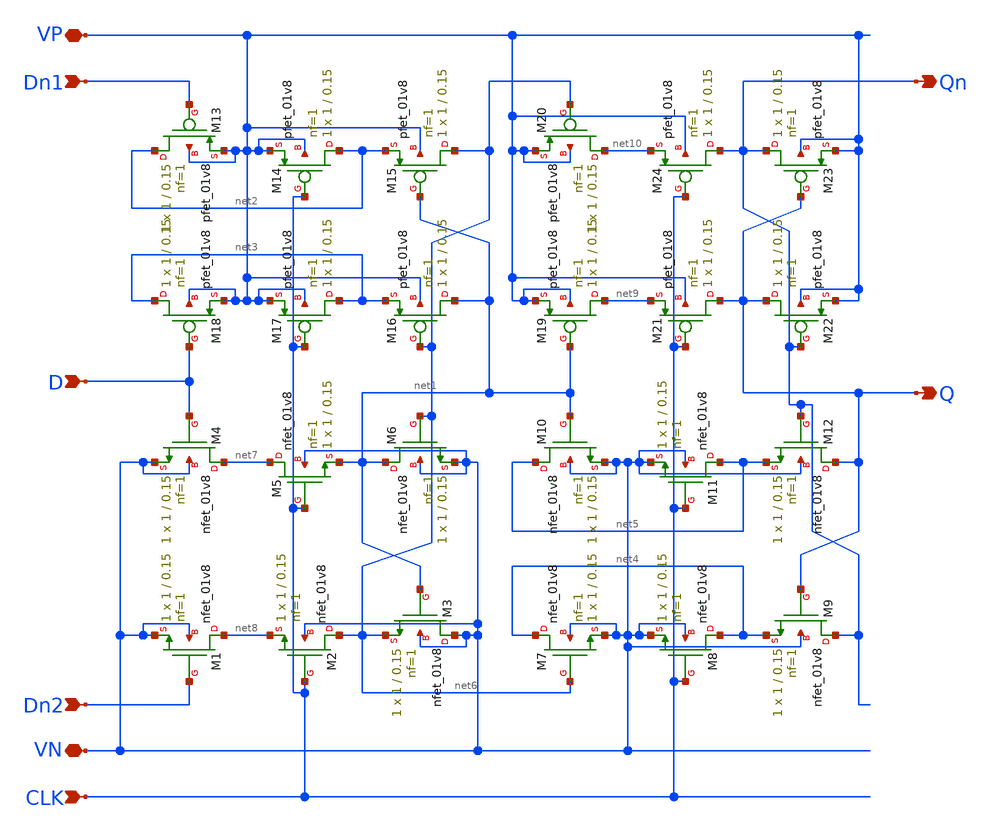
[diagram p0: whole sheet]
** sch_path: projects/negdff/xschem_ngspice/negdff2.sch
**.subckt negdff2 D Dn1 Dn2 Q Qn CLK VP VN
*.ipin D
*.ipin Dn1
*.ipin Dn2
*.opin Q
*.opin Qn
*.ipin CLK
*.iopin VP
*.iopin VN
XM1 net8 Dn2 VN VN sky130_fd_pr__nfet_01v8 L=0.15 W=1 nf=1 ad='int((nf+1)/2) * W/nf * 0.29' as='int((nf+2)/2) * W/nf * 0.29'
+ pd='2*int((nf+1)/2) * (W/nf + 0.29)' ps='2*int((nf+2)/2) * (W/nf + 0.29)' nrd='0.29 / W' nrs='0.29 / W'
+ sa=0 sb=0 sd=0 mult=1 m=1
XM2 net6 CLK net8 VN sky130_fd_pr__nfet_01v8 L=0.15 W=1 nf=1 ad='int((nf+1)/2) * W/nf * 0.29' as='int((nf+2)/2) * W/nf * 0.29'
+ pd='2*int((nf+1)/2) * (W/nf + 0.29)' ps='2*int((nf+2)/2) * (W/nf + 0.29)' nrd='0.29 / W' nrs='0.29 / W'
+ sa=0 sb=0 sd=0 mult=1 m=1
XM3 VN net1 net6 VN sky130_fd_pr__nfet_01v8 L=0.15 W=1 nf=1 ad='int((nf+1)/2) * W/nf * 0.29' as='int((nf+2)/2) * W/nf * 0.29'
+ pd='2*int((nf+1)/2) * (W/nf + 0.29)' ps='2*int((nf+2)/2) * (W/nf + 0.29)' nrd='0.29 / W' nrs='0.29 / W'
+ sa=0 sb=0 sd=0 mult=1 m=1
XM4 net7 D VN VN sky130_fd_pr__nfet_01v8 L=0.15 W=1 nf=1 ad='int((nf+1)/2) * W/nf * 0.29' as='int((nf+2)/2) * W/nf * 0.29'
+ pd='2*int((nf+1)/2) * (W/nf + 0.29)' ps='2*int((nf+2)/2) * (W/nf + 0.29)' nrd='0.29 / W' nrs='0.29 / W'
+ sa=0 sb=0 sd=0 mult=1 m=1
XM5 net7 CLK net1 VN sky130_fd_pr__nfet_01v8 L=0.15 W=1 nf=1 ad='int((nf+1)/2) * W/nf * 0.29' as='int((nf+2)/2) * W/nf * 0.29'
+ pd='2*int((nf+1)/2) * (W/nf + 0.29)' ps='2*int((nf+2)/2) * (W/nf + 0.29)' nrd='0.29 / W' nrs='0.29 / W'
+ sa=0 sb=0 sd=0 mult=1 m=1
XM6 net1 net6 VN VN sky130_fd_pr__nfet_01v8 L=0.15 W=1 nf=1 ad='int((nf+1)/2) * W/nf * 0.29' as='int((nf+2)/2) * W/nf * 0.29'
+ pd='2*int((nf+1)/2) * (W/nf + 0.29)' ps='2*int((nf+2)/2) * (W/nf + 0.29)' nrd='0.29 / W' nrs='0.29 / W'
+ sa=0 sb=0 sd=0 mult=1 m=1
XM7 net4 net6 VN VN sky130_fd_pr__nfet_01v8 L=0.15 W=1 nf=1 ad='int((nf+1)/2) * W/nf * 0.29' as='int((nf+2)/2) * W/nf * 0.29'
+ pd='2*int((nf+1)/2) * (W/nf + 0.29)' ps='2*int((nf+2)/2) * (W/nf + 0.29)' nrd='0.29 / W' nrs='0.29 / W'
+ sa=0 sb=0 sd=0 mult=1 m=1
XM8 net4 CLK VN VN sky130_fd_pr__nfet_01v8 L=0.15 W=1 nf=1 ad='int((nf+1)/2) * W/nf * 0.29' as='int((nf+2)/2) * W/nf * 0.29'
+ pd='2*int((nf+1)/2) * (W/nf + 0.29)' ps='2*int((nf+2)/2) * (W/nf + 0.29)' nrd='0.29 / W' nrs='0.29 / W'
+ sa=0 sb=0 sd=0 mult=1 m=1
XM9 Qn Q net4 VN sky130_fd_pr__nfet_01v8 L=0.15 W=1 nf=1 ad='int((nf+1)/2) * W/nf * 0.29' as='int((nf+2)/2) * W/nf * 0.29'
+ pd='2*int((nf+1)/2) * (W/nf + 0.29)' ps='2*int((nf+2)/2) * (W/nf + 0.29)' nrd='0.29 / W' nrs='0.29 / W'
+ sa=0 sb=0 sd=0 mult=1 m=1
XM10 net5 net1 VN VN sky130_fd_pr__nfet_01v8 L=0.15 W=1 nf=1 ad='int((nf+1)/2) * W/nf * 0.29' as='int((nf+2)/2) * W/nf * 0.29'
+ pd='2*int((nf+1)/2) * (W/nf + 0.29)' ps='2*int((nf+2)/2) * (W/nf + 0.29)' nrd='0.29 / W' nrs='0.29 / W'
+ sa=0 sb=0 sd=0 mult=1 m=1
XM11 net5 CLK VN VN sky130_fd_pr__nfet_01v8 L=0.15 W=1 nf=1 ad='int((nf+1)/2) * W/nf * 0.29' as='int((nf+2)/2) * W/nf * 0.29'
+ pd='2*int((nf+1)/2) * (W/nf + 0.29)' ps='2*int((nf+2)/2) * (W/nf + 0.29)' nrd='0.29 / W' nrs='0.29 / W'
+ sa=0 sb=0 sd=0 mult=1 m=1
XM12 Q Qn net5 VN sky130_fd_pr__nfet_01v8 L=0.15 W=1 nf=1 ad='int((nf+1)/2) * W/nf * 0.29' as='int((nf+2)/2) * W/nf * 0.29'
+ pd='2*int((nf+1)/2) * (W/nf + 0.29)' ps='2*int((nf+2)/2) * (W/nf + 0.29)' nrd='0.29 / W' nrs='0.29 / W'
+ sa=0 sb=0 sd=0 mult=1 m=1
XM13 net2 Dn1 VP VP sky130_fd_pr__pfet_01v8 L=0.15 W=1 nf=1 ad='int((nf+1)/2) * W/nf * 0.29' as='int((nf+2)/2) * W/nf * 0.29'
+ pd='2*int((nf+1)/2) * (W/nf + 0.29)' ps='2*int((nf+2)/2) * (W/nf + 0.29)' nrd='0.29 / W' nrs='0.29 / W'
+ sa=0 sb=0 sd=0 mult=1 m=1
XM14 net2 CLK VP VP sky130_fd_pr__pfet_01v8 L=0.15 W=1 nf=1 ad='int((nf+1)/2) * W/nf * 0.29' as='int((nf+2)/2) * W/nf * 0.29'
+ pd='2*int((nf+1)/2) * (W/nf + 0.29)' ps='2*int((nf+2)/2) * (W/nf + 0.29)' nrd='0.29 / W' nrs='0.29 / W'
+ sa=0 sb=0 sd=0 mult=1 m=1
XM15 net6 net1 net2 VP sky130_fd_pr__pfet_01v8 L=0.15 W=1 nf=1 ad='int((nf+1)/2) * W/nf * 0.29' as='int((nf+2)/2) * W/nf * 0.29'
+ pd='2*int((nf+1)/2) * (W/nf + 0.29)' ps='2*int((nf+2)/2) * (W/nf + 0.29)' nrd='0.29 / W' nrs='0.29 / W'
+ sa=0 sb=0 sd=0 mult=1 m=1
XM16 net1 net6 net3 VP sky130_fd_pr__pfet_01v8 L=0.15 W=1 nf=1 ad='int((nf+1)/2) * W/nf * 0.29' as='int((nf+2)/2) * W/nf * 0.29'
+ pd='2*int((nf+1)/2) * (W/nf + 0.29)' ps='2*int((nf+2)/2) * (W/nf + 0.29)' nrd='0.29 / W' nrs='0.29 / W'
+ sa=0 sb=0 sd=0 mult=1 m=1
XM17 net3 CLK VP VP sky130_fd_pr__pfet_01v8 L=0.15 W=1 nf=1 ad='int((nf+1)/2) * W/nf * 0.29' as='int((nf+2)/2) * W/nf * 0.29'
+ pd='2*int((nf+1)/2) * (W/nf + 0.29)' ps='2*int((nf+2)/2) * (W/nf + 0.29)' nrd='0.29 / W' nrs='0.29 / W'
+ sa=0 sb=0 sd=0 mult=1 m=1
XM18 net3 D VP VP sky130_fd_pr__pfet_01v8 L=0.15 W=1 nf=1 ad='int((nf+1)/2) * W/nf * 0.29' as='int((nf+2)/2) * W/nf * 0.29'
+ pd='2*int((nf+1)/2) * (W/nf + 0.29)' ps='2*int((nf+2)/2) * (W/nf + 0.29)' nrd='0.29 / W' nrs='0.29 / W'
+ sa=0 sb=0 sd=0 mult=1 m=1
XM19 net9 net1 VP VP sky130_fd_pr__pfet_01v8 L=0.15 W=1 nf=1 ad='int((nf+1)/2) * W/nf * 0.29' as='int((nf+2)/2) * W/nf * 0.29'
+ pd='2*int((nf+1)/2) * (W/nf + 0.29)' ps='2*int((nf+2)/2) * (W/nf + 0.29)' nrd='0.29 / W' nrs='0.29 / W'
+ sa=0 sb=0 sd=0 mult=1 m=1
XM20 net10 net6 VP VP sky130_fd_pr__pfet_01v8 L=0.15 W=1 nf=1 ad='int((nf+1)/2) * W/nf * 0.29' as='int((nf+2)/2) * W/nf * 0.29'
+ pd='2*int((nf+1)/2) * (W/nf + 0.29)' ps='2*int((nf+2)/2) * (W/nf + 0.29)' nrd='0.29 / W' nrs='0.29 / W'
+ sa=0 sb=0 sd=0 mult=1 m=1
XM21 Q CLK net9 VP sky130_fd_pr__pfet_01v8 L=0.15 W=1 nf=1 ad='int((nf+1)/2) * W/nf * 0.29' as='int((nf+2)/2) * W/nf * 0.29'
+ pd='2*int((nf+1)/2) * (W/nf + 0.29)' ps='2*int((nf+2)/2) * (W/nf + 0.29)' nrd='0.29 / W' nrs='0.29 / W'
+ sa=0 sb=0 sd=0 mult=1 m=1
XM22 Q Qn VP VP sky130_fd_pr__pfet_01v8 L=0.15 W=1 nf=1 ad='int((nf+1)/2) * W/nf * 0.29' as='int((nf+2)/2) * W/nf * 0.29'
+ pd='2*int((nf+1)/2) * (W/nf + 0.29)' ps='2*int((nf+2)/2) * (W/nf + 0.29)' nrd='0.29 / W' nrs='0.29 / W'
+ sa=0 sb=0 sd=0 mult=1 m=1
XM23 Qn Q VP VP sky130_fd_pr__pfet_01v8 L=0.15 W=1 nf=1 ad='int((nf+1)/2) * W/nf * 0.29' as='int((nf+2)/2) * W/nf * 0.29'
+ pd='2*int((nf+1)/2) * (W/nf + 0.29)' ps='2*int((nf+2)/2) * (W/nf + 0.29)' nrd='0.29 / W' nrs='0.29 / W'
+ sa=0 sb=0 sd=0 mult=1 m=1
XM24 Qn CLK net10 VP sky130_fd_pr__pfet_01v8 L=0.15 W=1 nf=1 ad='int((nf+1)/2) * W/nf * 0.29' as='int((nf+2)/2) * W/nf * 0.29'
+ pd='2*int((nf+1)/2) * (W/nf + 0.29)' ps='2*int((nf+2)/2) * (W/nf + 0.29)' nrd='0.29 / W' nrs='0.29 / W'
+ sa=0 sb=0 sd=0 mult=1 m=1
**.ends
.end
